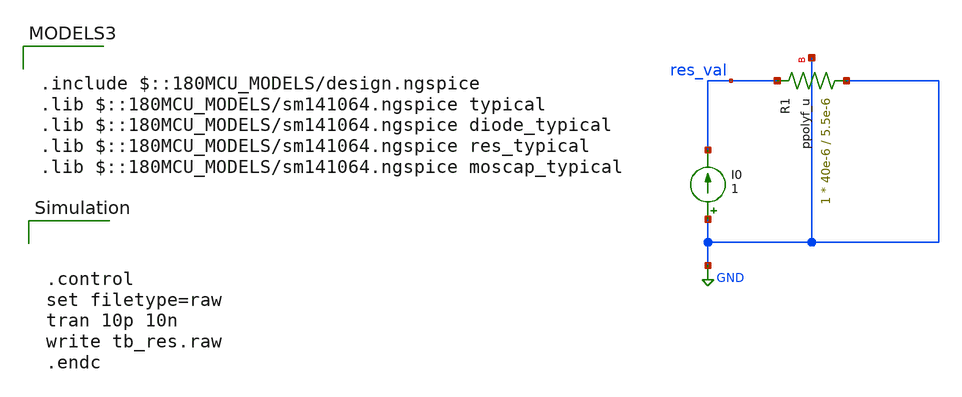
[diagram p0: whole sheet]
** sch_path: designs/libs/secondary_esd/tb_res.sch
**.subckt tb_res
I0 GND res_val 1
XR1 GND res_val GND ppolyf_u r_width=40e-6 r_length=5.5e-6 m=1
**** begin user architecture code



.control
set filetype=raw
tran 10p 10n
write tb_res.raw
.endc



.include $::180MCU_MODELS/design.ngspice
.lib $::180MCU_MODELS/sm141064.ngspice typical
.lib $::180MCU_MODELS/sm141064.ngspice diode_typical
.lib $::180MCU_MODELS/sm141064.ngspice res_typical
.lib $::180MCU_MODELS/sm141064.ngspice moscap_typical

**** end user architecture code
**.ends
.GLOBAL GND
.end
